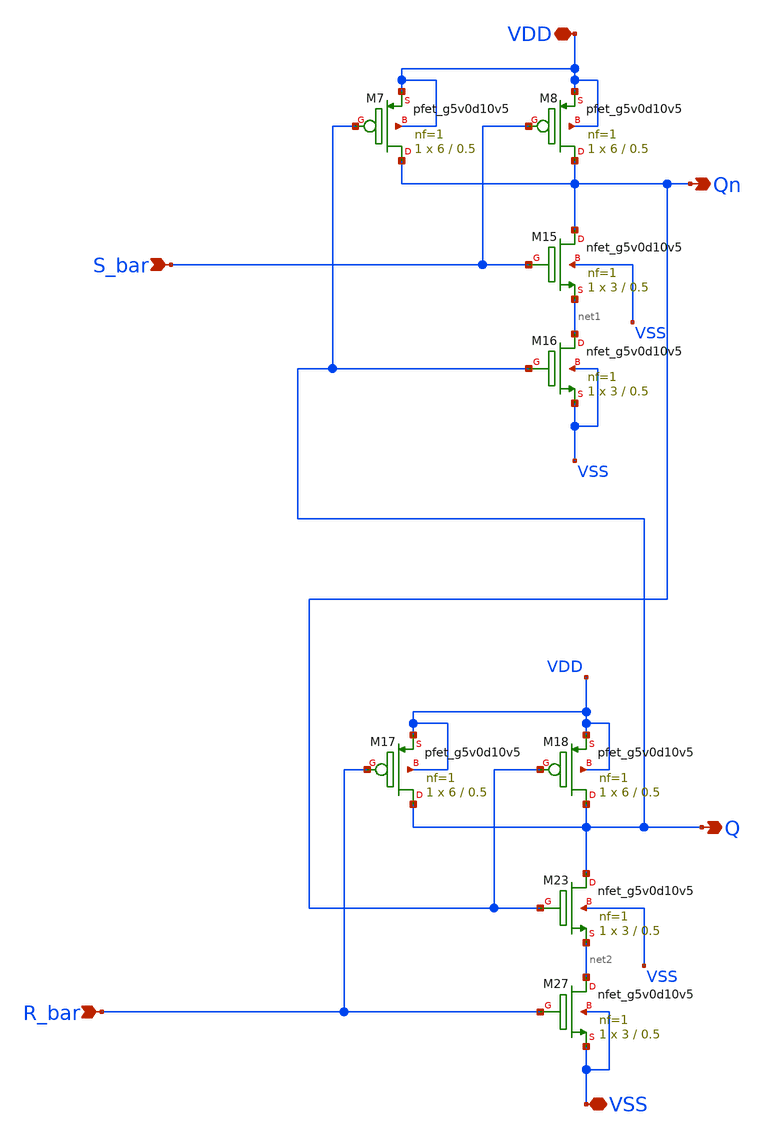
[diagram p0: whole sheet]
** sch_path: SKY130/SAR-ADC/SAR-ADC_5.0V/SR.sch
**.subckt SR VDD Qn Q S_bar R_bar VSS
*.iopin VDD
*.opin Qn
*.opin Q
*.ipin S_bar
*.ipin R_bar
*.iopin VSS
XM7 Qn Q VDD VDD sky130_fd_pr__pfet_g5v0d10v5 L=0.5 W=6 nf=1 ad='int((1 + 1)/2) * 6 / 1 * 0.29' as='int((1 + 2)/2) * 6 / 1 * 0.29'
+ pd='2*int((1 + 1)/2) * (6 / 1 + 0.29)' ps='2*int((1 + 2)/2) * (6 / 1 + 0.29)' nrd='0.29 / 6 ' nrs='0.29 / 6 '
+ sa=0 sb=0 sd=0 mult=1 m=1
XM8 Qn S_bar VDD VDD sky130_fd_pr__pfet_g5v0d10v5 L=0.5 W=6 nf=1 ad='int((1 + 1)/2) * 6 / 1 * 0.29' as='int((1 + 2)/2) * 6 / 1 * 0.29'
+ pd='2*int((1 + 1)/2) * (6 / 1 + 0.29)' ps='2*int((1 + 2)/2) * (6 / 1 + 0.29)' nrd='0.29 / 6 ' nrs='0.29 / 6 '
+ sa=0 sb=0 sd=0 mult=1 m=1
XM15 Qn S_bar net1 VSS sky130_fd_pr__nfet_g5v0d10v5 L=0.5 W=3 nf=1 ad='int((1 + 1)/2) * 3 / 1 * 0.29'
+ as='int((1 + 2)/2) * 3 / 1 * 0.29' pd='2*int((1 + 1)/2) * (3 / 1 + 0.29)' ps='2*int((1 + 2)/2) * (3 / 1 + 0.29)'
+ nrd='0.29 / 3 ' nrs='0.29 / 3 ' sa=0 sb=0 sd=0 mult=1 m=1
XM16 net1 Q VSS VSS sky130_fd_pr__nfet_g5v0d10v5 L=0.5 W=3 nf=1 ad='int((1 + 1)/2) * 3 / 1 * 0.29' as='int((1 + 2)/2) * 3 / 1 * 0.29'
+ pd='2*int((1 + 1)/2) * (3 / 1 + 0.29)' ps='2*int((1 + 2)/2) * (3 / 1 + 0.29)' nrd='0.29 / 3 ' nrs='0.29 / 3 '
+ sa=0 sb=0 sd=0 mult=1 m=1
XM17 Q R_bar VDD VDD sky130_fd_pr__pfet_g5v0d10v5 L=0.5 W=6 nf=1 ad='int((1 + 1)/2) * 6 / 1 * 0.29' as='int((1 + 2)/2) * 6 / 1 * 0.29'
+ pd='2*int((1 + 1)/2) * (6 / 1 + 0.29)' ps='2*int((1 + 2)/2) * (6 / 1 + 0.29)' nrd='0.29 / 6 ' nrs='0.29 / 6 '
+ sa=0 sb=0 sd=0 mult=1 m=1
XM18 Q Qn VDD VDD sky130_fd_pr__pfet_g5v0d10v5 L=0.5 W=6 nf=1 ad='int((1 + 1)/2) * 6 / 1 * 0.29' as='int((1 + 2)/2) * 6 / 1 * 0.29'
+ pd='2*int((1 + 1)/2) * (6 / 1 + 0.29)' ps='2*int((1 + 2)/2) * (6 / 1 + 0.29)' nrd='0.29 / 6 ' nrs='0.29 / 6 '
+ sa=0 sb=0 sd=0 mult=1 m=1
XM23 Q Qn net2 VSS sky130_fd_pr__nfet_g5v0d10v5 L=0.5 W=3 nf=1 ad='int((1 + 1)/2) * 3 / 1 * 0.29' as='int((1 + 2)/2) * 3 / 1 * 0.29'
+ pd='2*int((1 + 1)/2) * (3 / 1 + 0.29)' ps='2*int((1 + 2)/2) * (3 / 1 + 0.29)' nrd='0.29 / 3 ' nrs='0.29 / 3 '
+ sa=0 sb=0 sd=0 mult=1 m=1
XM27 net2 R_bar VSS VSS sky130_fd_pr__nfet_g5v0d10v5 L=0.5 W=3 nf=1 ad='int((1 + 1)/2) * 3 / 1 * 0.29'
+ as='int((1 + 2)/2) * 3 / 1 * 0.29' pd='2*int((1 + 1)/2) * (3 / 1 + 0.29)' ps='2*int((1 + 2)/2) * (3 / 1 + 0.29)'
+ nrd='0.29 / 3 ' nrs='0.29 / 3 ' sa=0 sb=0 sd=0 mult=1 m=1
**.ends
.end
